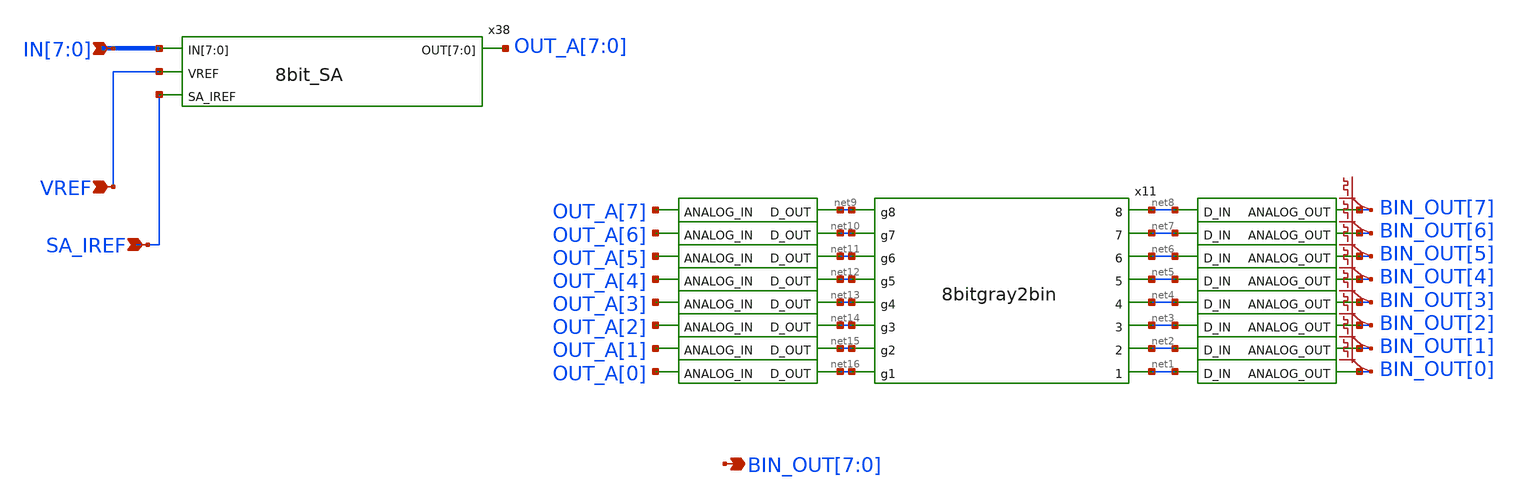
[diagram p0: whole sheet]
** sch_path: xschem/8bit_SA_converter.sch
**.subckt 8bit_SA_converter IN[7],IN[6],IN[5],IN[4],IN[3],IN[2],IN[1],IN[0] VREF
*+ BIN_OUT[7],BIN_OUT[6],BIN_OUT[5],BIN_OUT[4],BIN_OUT[3],BIN_OUT[2],BIN_OUT[1],BIN_OUT[0] SA_IREF
*.ipin IN[7],IN[6],IN[5],IN[4],IN[3],IN[2],IN[1],IN[0]
*.ipin VREF
*.opin BIN_OUT[7],BIN_OUT[6],BIN_OUT[5],BIN_OUT[4],BIN_OUT[3],BIN_OUT[2],BIN_OUT[1],BIN_OUT[0]
*.ipin SA_IREF
x38 IN[7] IN[6] IN[5] IN[4] IN[3] IN[2] IN[1] IN[0] VREF SA_IREF OUT_A[7] OUT_A[6] OUT_A[5] OUT_A[4]
+ OUT_A[3] OUT_A[2] OUT_A[1] OUT_A[0] 8bit_SA
x11 net8 net9 net10 net7 net6 net11 net5 net12 net13 net4 net3 net14 net15 net2 net16 net1
+ 8bitgray2bin
x12 BIN_OUT[7] net8 dac_bridge
x13 BIN_OUT[6] net7 dac_bridge
x14 BIN_OUT[5] net6 dac_bridge
x16 BIN_OUT[4] net5 dac_bridge
x17 BIN_OUT[3] net4 dac_bridge
x18 BIN_OUT[2] net3 dac_bridge
x19 BIN_OUT[1] net2 dac_bridge
x37 BIN_OUT[0] net1 dac_bridge
x39 net9 OUT_A[7] adc_bridge
x40 net10 OUT_A[6] adc_bridge
x41 net11 OUT_A[5] adc_bridge
x42 net12 OUT_A[4] adc_bridge
x43 net13 OUT_A[3] adc_bridge
x44 net14 OUT_A[2] adc_bridge
x45 net15 OUT_A[1] adc_bridge
x46 net16 OUT_A[0] adc_bridge
.save v(bin_out[7])
.save v(bin_out[6])
.save v(bin_out[5])
.save v(bin_out[4])
.save v(bin_out[3])
.save v(bin_out[2])
.save v(bin_out[1])
.save v(bin_out[0])
**.ends

* expanding   symbol:  8bit_SA.sym # of pins=4
** sym_path: xschem/8bit_SA.sym
** sch_path: xschem/8bit_SA.sch
.subckt 8bit_SA IN[7] IN[6] IN[5] IN[4] IN[3] IN[2] IN[1] IN[0] VREF SA_IREF OUT[7] OUT[6] OUT[5]
+ OUT[4] OUT[3] OUT[2] OUT[1] OUT[0]
*.ipin IN[7],IN[6],IN[5],IN[4],IN[3],IN[2],IN[1],IN[0]
*.ipin VREF
*.opin OUT[7],OUT[6],OUT[5],OUT[4],OUT[3],OUT[2],OUT[1],OUT[0]
*.ipin SA_IREF
x2 OUT[7] VREF IN[7] SA_IREF sens_amp
x3 OUT[6] VREF IN[6] SA_IREF sens_amp
x4 OUT[5] VREF IN[5] SA_IREF sens_amp
x5 OUT[4] VREF IN[4] SA_IREF sens_amp
x6 OUT[3] VREF IN[3] SA_IREF sens_amp
x7 OUT[2] net1 IN[2] SA_IREF sens_amp
x8 OUT[1] VREF IN[1] SA_IREF sens_amp
x9 OUT[0] VREF IN[0] SA_IREF sens_amp
.ends


* expanding   symbol:  adc/8bitgray2bin.sym # of pins=16
** sym_path: xschem/adc/8bitgray2bin.sym
** sch_path: xschem/adc/8bitgray2bin.sch
.subckt 8bitgray2bin 8 g8 g7 7 6 g6 5 g5 g4 4 3 g3 g2 2 g1 1
*.opin 7
*.opin 6
*.opin 5
*.opin 4
*.opin 3
*.opin 2
*.opin 1
*.opin 8
*.ipin g5
*.ipin g4
*.ipin g3
*.ipin g8
*.ipin g7
*.ipin g6
*.ipin g2
*.ipin g1
**** begin user architecture code


* lsb first.
a1 [g1 g2 g3 g4 g5 g6 g7 g8] [1 2 3 4 5 6 7 8] gray2bin_lut
.model gray2bin_lut d_genlut(rise_delay=[1p 1p] fall_delay=[1p 1p]  input_load=[1p 1p]
+ input_delay=[0 0]
+ table_values=01101001100101101001011001101001100101100110100101101001100101101001011001101001011010011001011001101001100101101001011001101001100101100110100101101001100101100110100110010110100101100110100101101001100101101001011001101001100101100110100101101001100101100011110011000011110000110011110011000011001111000011110011000011110000110011110000111100110000110011110011000011110000110011110011000011001111000011110011000011001111001100001111000011001111000011110011000011110000110011110011000011001111000011110011000011000011111111000011110000000011111111000000001111000011111111000011110000000011110000111111110000000011111111000011110000000011111111000000001111000011111111000000001111111100001111000000001111000011111111000011110000000011111111000000001111000011111111000000000000111111111111111100000000111111110000000000000000111111111111111100000000000000001111111100000000111111111111111100000000111111110000000000000000111111110000000011111111111111110000000000000000111111111111111100000000111111110000000000000000111111110000000000000000111111111111111111111111111111110000000000000000111111111111111100000000000000000000000000000000111111111111111111111111111111110000000000000000000000000000000011111111111111110000000000000000111111111111111111111111111111110000000000000000000000000000000000000000000000001111111111111111111111111111111111111111111111111111111111111111000000000000000000000000000000001111111111111111111111111111111100000000000000000000000000000000000000000000000000000000000000001111111111111111111111111111111100000000000000000000000000000000000000000000000000000000000000001111111111111111111111111111111111111111111111111111111111111111111111111111111111111111111111111111111111111111111111111111111100000000000000000000000000000000000000000000000000000000000000000000000000000000000000000000000000000000000000000000000000000000000000000000000000000000000000000000000000000000000000000000000011111111111111111111111111111111111111111111111111111111111111111111111111111111111111111111111111111111111111111111111111111111)




**** end user architecture code
.ends


* expanding   symbol:  digital_prims/dac_bridge.sym # of pins=2
** sym_path: xschem/digital_prims/dac_bridge.sym
** sch_path: xschem/digital_prims/dac_bridge.sch
.subckt dac_bridge ANALOG_OUT D_IN
*.ipin D_IN
*.opin ANALOG_OUT
**** begin user architecture code


abridge_d [D_IN] [ANALOG_OUT] dac_buff
.model dac_buff dac_bridge(out_high=1.8)


**** end user architecture code
.ends


* expanding   symbol:  digital_prims/adc_bridge.sym # of pins=2
** sym_path: xschem/digital_prims/adc_bridge.sym
** sch_path: xschem/digital_prims/adc_bridge.sch
.subckt adc_bridge D_OUT ANALOG_IN
*.ipin ANALOG_IN
*.opin D_OUT
**** begin user architecture code


abridge [ANALOG_IN] [D_OUT] adc_buff
.model adc_buff adc_bridge(in_low=0.9 in_high =0.9)


**** end user architecture code
.ends


* expanding   symbol:  sens_amp.sym # of pins=4
** sym_path: xschem/sens_amp.sym
** sch_path: xschem/sens_amp.sch
.subckt sens_amp OUT REF V_IN SA_IREF
*.ipin REF
*.ipin V_IN
*.opin OUT
*.ipin SA_IREF
XM5 net1 GN VDD VDD sky130_fd_pr__pfet_01v8_lvt L=0.5 W=1 nf=1 ad='W * 0.29' as='W * 0.29' pd='2*(W + 0.29)'
+ ps='2*(W + 0.29)' nrd=0 nrs=0 sa=0 sb=0 sd=0 mult=1 m=1
XM6 GN GN VDD VDD sky130_fd_pr__pfet_01v8_lvt L=0.5 W=1 nf=1 ad='W * 0.29' as='W * 0.29' pd='2*(W + 0.29)'
+ ps='2*(W + 0.29)' nrd=0 nrs=0 sa=0 sb=0 sd=0 mult=1 m=1
XM23 net1 V_IN net2 GND sky130_fd_pr__nfet_01v8_lvt L=0.15 W=4 nf=1 ad='W * 0.29' as='W * 0.29' pd='2*(W + 0.29)'
+ ps='2*(W + 0.29)' nrd=0 nrs=0 sa=0 sb=0 sd=0 mult=1 m=1
XM16 GN REF net2 GND sky130_fd_pr__nfet_01v8_lvt L=0.15 W=4 nf=1 ad='W * 0.29' as='W * 0.29' pd='2*(W + 0.29)'
+ ps='2*(W + 0.29)' nrd=0 nrs=0 sa=0 sb=0 sd=0 mult=1 m=1
XM1 OUT net1 GND GND sky130_fd_pr__nfet_01v8_lvt L=0.15 W=1 nf=1 ad='W * 0.29' as='W * 0.29' pd='2*(W + 0.29)'
+ ps='2*(W + 0.29)' nrd=0 nrs=0 sa=0 sb=0 sd=0 mult=1 m=1
XM2 OUT net1 VDD VDD sky130_fd_pr__pfet_01v8_lvt L=0.35 W=3 nf=1 ad='W * 0.29' as='W * 0.29' pd='2*(W + 0.29)'
+ ps='2*(W + 0.29)' nrd=0 nrs=0 sa=0 sb=0 sd=0 mult=1 m=1
XM3 net3 SA_IREF GND GND sky130_fd_pr__nfet_01v8_lvt L=1 W=0.5 nf=1 ad='W * 0.29' as='W * 0.29' pd='2*(W + 0.29)'
+ ps='2*(W + 0.29)' nrd=0 nrs=0 sa=0 sb=0 sd=0 mult=1 m=1
Vmeas net2 net3 0
.save i(vmeas)
.ends

.GLOBAL GND
.end
